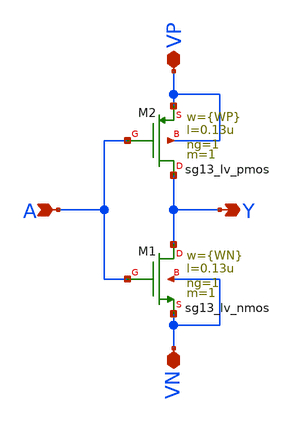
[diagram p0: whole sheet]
** sch_path: xschem/inv.sch
**.subckt inv A Y VP VN
*.ipin A
*.opin Y
*.iopin VP
*.iopin VN
XM1 Y A VN VN sg13_lv_nmos w={WN} l=0.13u ng=1 m=1 mm_ok=1
XM2 Y A VP VP sg13_lv_pmos w={WP} l=0.13u ng=1 m=1 mm_ok=1
**.ends
.end
